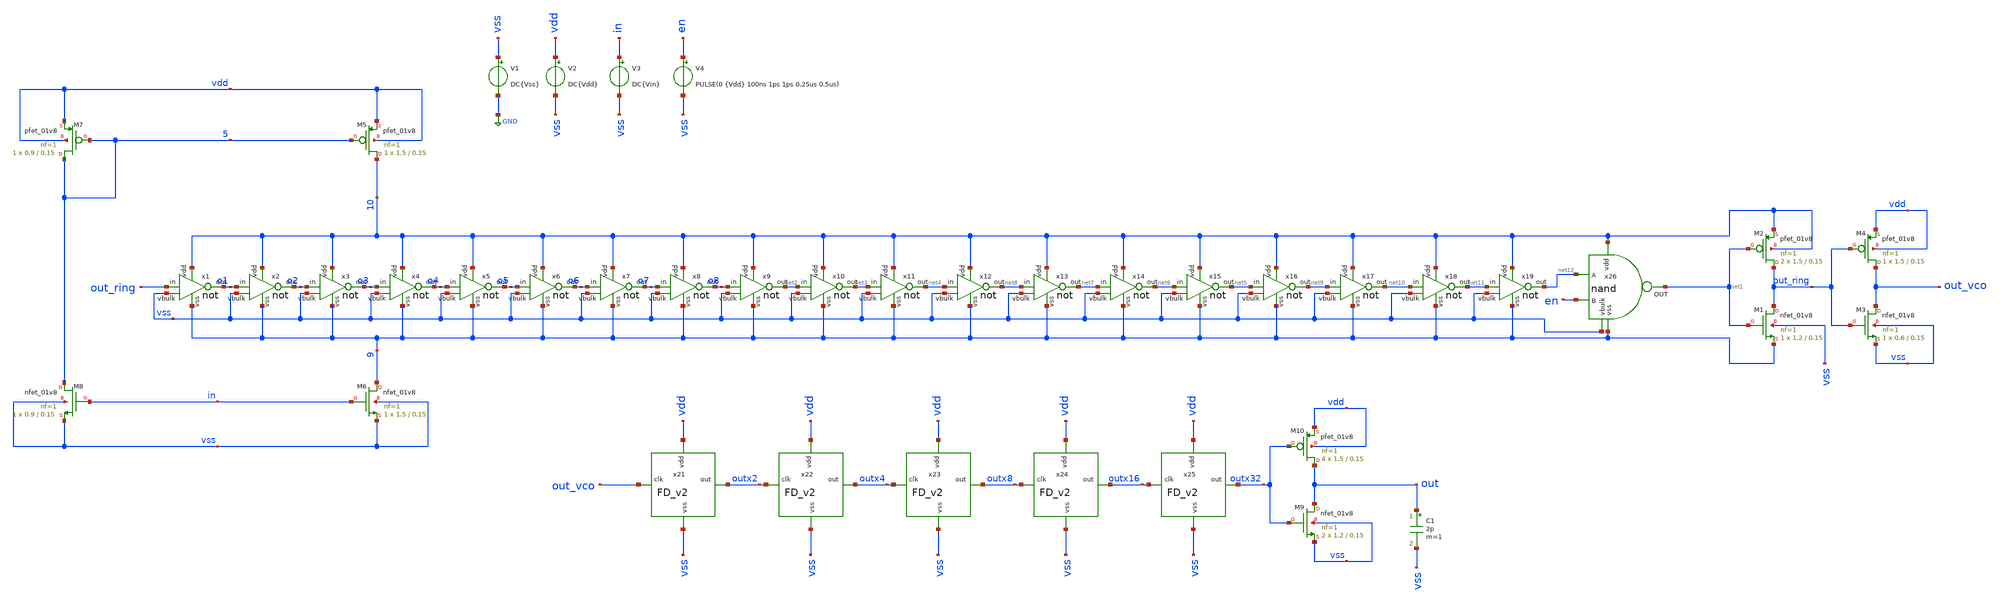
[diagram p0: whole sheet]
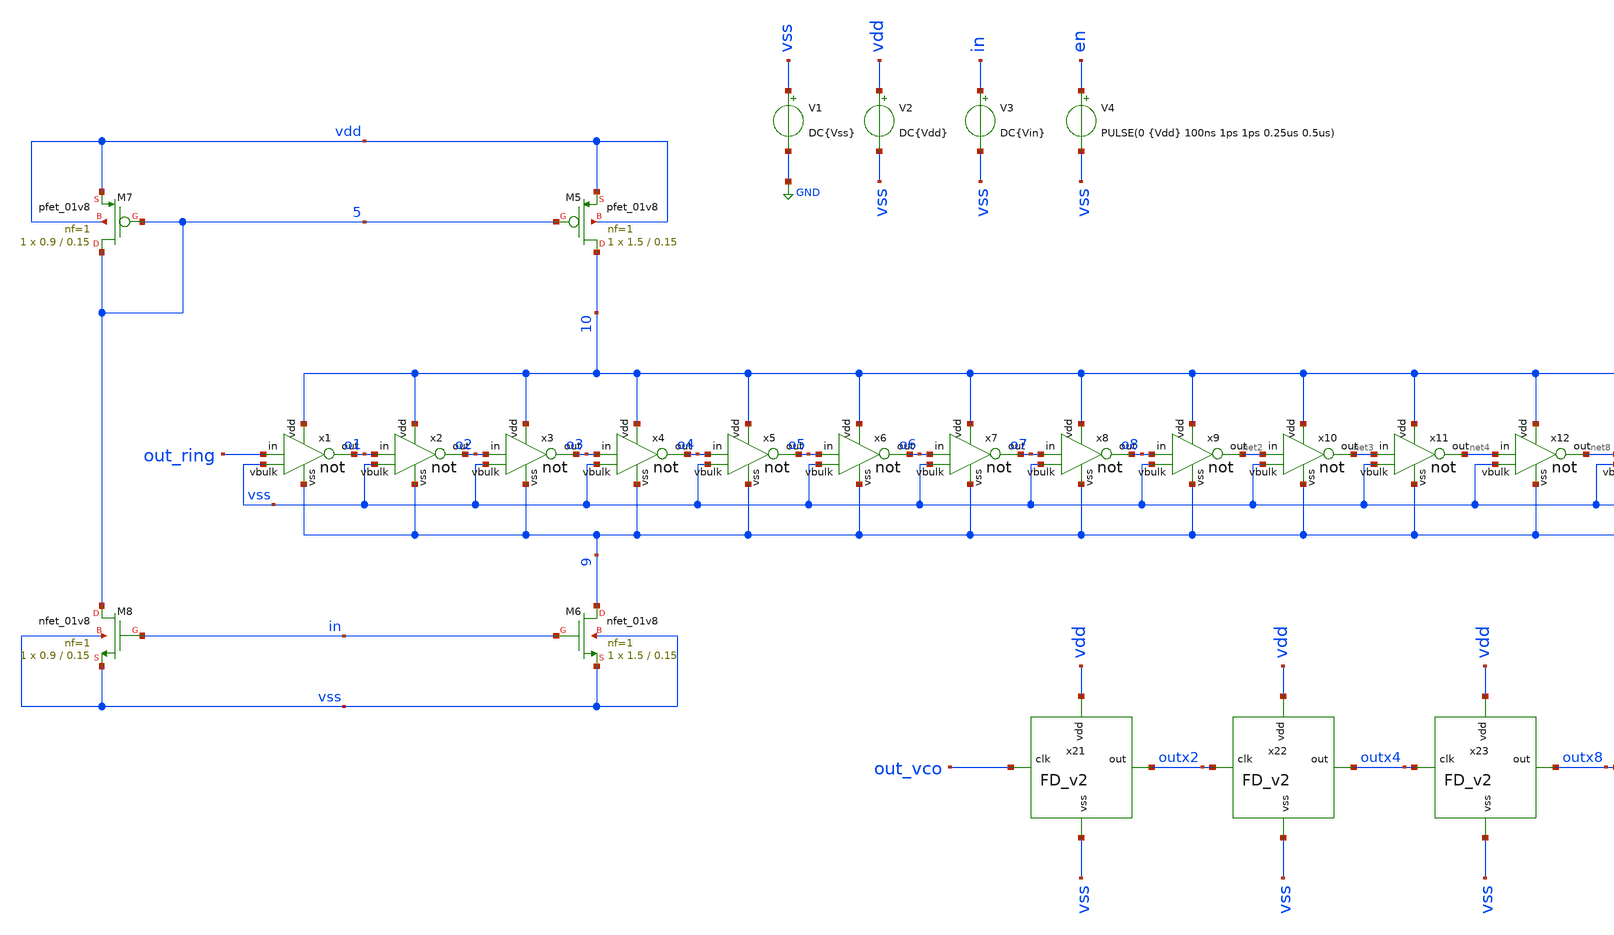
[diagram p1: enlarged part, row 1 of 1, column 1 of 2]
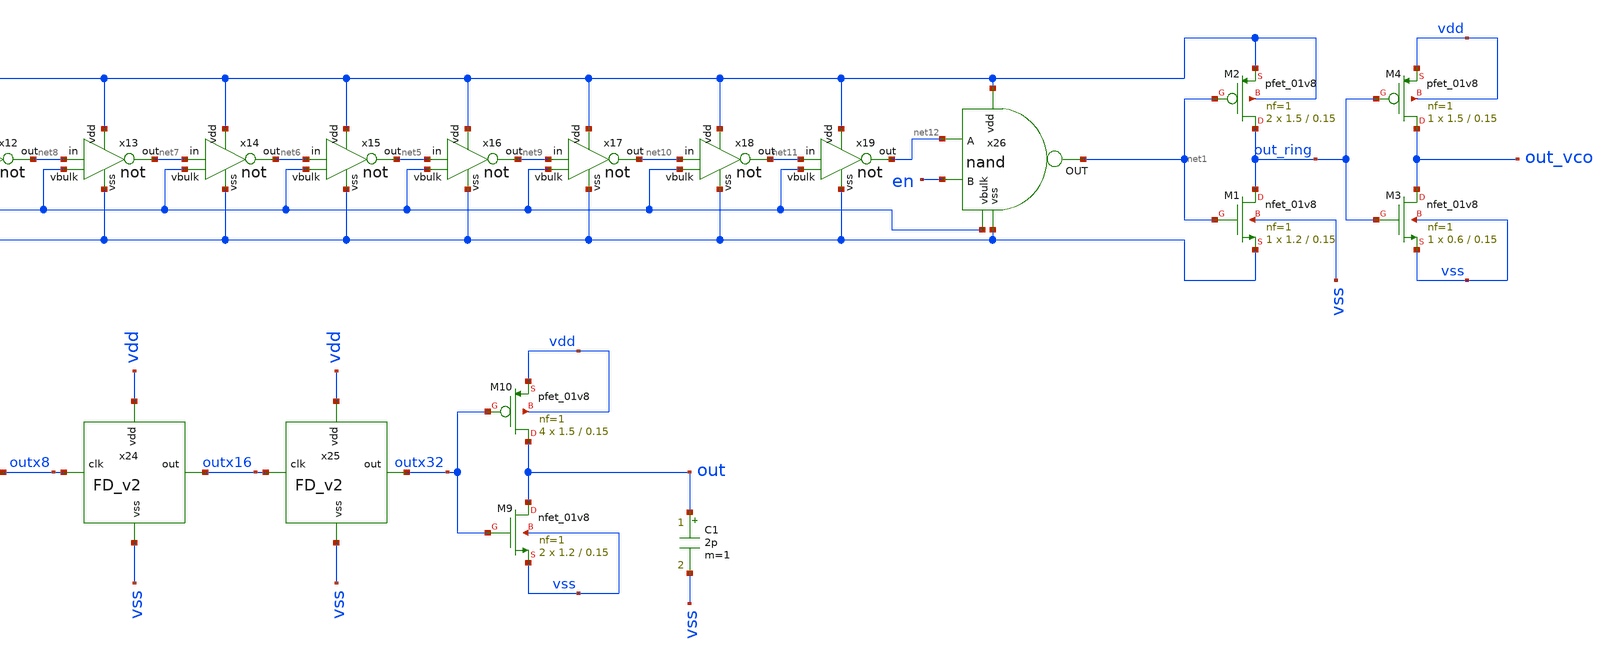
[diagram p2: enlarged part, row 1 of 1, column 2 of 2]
** sch_path: xsch/sch/ring_vco/ring_vco.sch
**.subckt ring_vco
x1 10 out_ring o1 9 vss not
V1 vss GND DC{Vss}
V2 vdd vss DC{Vdd}
x2 10 o1 o2 9 vss not
x3 10 o2 o3 9 vss not
x4 10 o3 o4 9 vss not
x5 10 o4 o5 9 vss not
x6 10 o5 o6 9 vss not
XM1 out_ring net1 9 vss sky130_fd_pr__nfet_01v8 L=0.15 W=1.2 nf=1 ad='W * 0.29' as='W * 0.29' pd='2 * (W + 0.29)'
+ ps='2 * (W + 0.29)' nrd='0.29 / W' nrs='0.29 / W' sa=0 sb=0 sd=0 mult=1 m=1
XM2 out_ring net1 10 10 sky130_fd_pr__pfet_01v8 L=0.15 W=1.5 nf=1 ad='W * 0.29' as='W * 0.29' pd='2 * (W + 0.29)'
+ ps='2 * (W + 0.29)' nrd='0.29 / W' nrs='0.29 / W' sa=0 sb=0 sd=0 mult=2 m=2
XM3 out_vco out_ring vss vss sky130_fd_pr__nfet_01v8 L=0.15 W=0.6 nf=1 ad='W * 0.29' as='W * 0.29' pd='2 * (W + 0.29)'
+ ps='2 * (W + 0.29)' nrd='0.29 / W' nrs='0.29 / W' sa=0 sb=0 sd=0 mult=1 m=1
XM4 out_vco out_ring vdd vdd sky130_fd_pr__pfet_01v8 L=0.15 W=1.5 nf=1 ad='W * 0.29' as='W * 0.29' pd='2 * (W + 0.29)'
+ ps='2 * (W + 0.29)' nrd='0.29 / W' nrs='0.29 / W' sa=0 sb=0 sd=0 mult=1 m=1
XM5 10 5 vdd vdd sky130_fd_pr__pfet_01v8 L=0.15 W=1.5 nf=1 ad='W * 0.29' as='W * 0.29' pd='2 * (W + 0.29)'
+ ps='2 * (W + 0.29)' nrd='0.29 / W' nrs='0.29 / W' sa=0 sb=0 sd=0 mult=1 m=1
XM6 9 in vss vss sky130_fd_pr__nfet_01v8 L=0.15 W=1.5 nf=1 ad='W * 0.29' as='W * 0.29' pd='2 * (W + 0.29)'
+ ps='2 * (W + 0.29)' nrd='0.29 / W' nrs='0.29 / W' sa=0 sb=0 sd=0 mult=1 m=1
XM7 5 5 vdd vdd sky130_fd_pr__pfet_01v8 L=0.15 W=0.9 nf=1 ad='W * 0.29' as='W * 0.29' pd='2 * (W + 0.29)'
+ ps='2 * (W + 0.29)' nrd='0.29 / W' nrs='0.29 / W' sa=0 sb=0 sd=0 mult=1 m=1
XM8 5 in vss vss sky130_fd_pr__nfet_01v8 L=0.15 W=0.9 nf=1 ad='W * 0.29' as='W * 0.29' pd='2 * (W + 0.29)'
+ ps='2 * (W + 0.29)' nrd='0.29 / W' nrs='0.29 / W' sa=0 sb=0 sd=0 mult=1 m=1
V3 in vss DC{Vin}
x7 10 o6 o7 9 vss not
x8 10 o7 o8 9 vss not
x9 10 o8 net2 9 vss not
x10 10 net2 net3 9 vss not
x11 10 net3 net4 9 vss not
x12 10 net4 net8 9 vss not
x13 10 net8 net7 9 vss not
x14 10 net7 net6 9 vss not
x15 10 net6 net5 9 vss not
x16 10 net5 net9 9 vss not
x17 10 net9 net10 9 vss not
x18 10 net10 net11 9 vss not
x19 10 net11 net12 9 vss not
x21 out_vco vss outx2 vdd FD_v2
x22 outx2 vss outx4 vdd FD_v2
x23 outx4 vss outx8 vdd FD_v2
x24 outx8 vss outx16 vdd FD_v2
x25 outx16 vss outx32 vdd FD_v2
C1 out vss 2p m=1
XM9 out outx32 vss vss sky130_fd_pr__nfet_01v8 L=0.15 W=1.2 nf=1 ad='W * 0.29' as='W * 0.29' pd='2 * (W + 0.29)'
+ ps='2 * (W + 0.29)' nrd='0.29 / W' nrs='0.29 / W' sa=0 sb=0 sd=0 mult=2 m=2
XM10 out outx32 vdd vdd sky130_fd_pr__pfet_01v8 L=0.15 W=1.5 nf=1 ad='W * 0.29' as='W * 0.29' pd='2 * (W + 0.29)'
+ ps='2 * (W + 0.29)' nrd='0.29 / W' nrs='0.29 / W' sa=0 sb=0 sd=0 mult=4 m=4
x26 10 net12 net1 en 9 vss nand
V4 en vss PULSE(0 {Vdd} 100ns 1ps 1ps 0.25us 0.5us)
**** begin user architecture code




* Circuit Parameters
.param vdd  = 1.8
.param vss  = 0.0
.param vin  = 1
.param iref = 200u
.options TEMP = 65.0

* Include Models
.lib /home/tools/repos_sky130/skywater-pdk/libraries/sky130_fd_pr_ngspice/latest/models/corners/sky130.lib TT

* OP Parameters & Singals to save
.save all  @M.X2.XM1.msky130_fd_pr__nfet_01v8[id] @M.X2.XM1.msky130_fd_pr__nfet_01v8[vth] @M.X2.XM1.msky130_fd_pr__nfet_01v8[vgs] @M.X2.XM1.msky130_fd_pr__nfet_01v8[vds] @M.X2.XM1.msky130_fd_pr__nfet_01v8[vdsat] @M.X2.XM1.msky130_fd_pr__nfet_01v8[gm] @M.X2.XM1.msky130_fd_pr__nfet_01v8[gds] @M.X2.XM1.msky130_fd_pr__nfet_01v8[cgs] @M.X2.XM1.msky130_fd_pr__nfet_01v8[cgd]  @M.X2.XM2.msky130_fd_pr__pfet_01v8[id] @M.X2.XM2.msky130_fd_pr__pfet_01v8[vth] @M.X2.XM2.msky130_fd_pr__pfet_01v8[vgs] @M.X2.XM2.msky130_fd_pr__pfet_01v8[vds] @M.X2.XM2.msky130_fd_pr__pfet_01v8[vdsat] @M.X2.XM2.msky130_fd_pr__pfet_01v8[gm] @M.X2.XM2.msky130_fd_pr__pfet_01v8[gds] @M.X2.XM1.msky130_fd_pr__nfet_01v8[cgs] @M.X2.XM1.msky130_fd_pr__nfet_01v8[cgd]  @M.XM6.msky130_fd_pr__nfet_01v8[id] @M.XM6.msky130_fd_pr__nfet_01v8[vth] @M.XM6.msky130_fd_pr__nfet_01v8[vgs] @M.XM6.msky130_fd_pr__nfet_01v8[vds] @M.XM6.msky130_fd_pr__nfet_01v8[vdsat] @M.XM6.msky130_fd_pr__nfet_01v8[gm] @M.XM6.msky130_fd_pr__nfet_01v8[gds] @M.XM6.msky130_fd_pr__nfet_01v8[cgs] @M.XM6.msky130_fd_pr__nfet_01v8[cgd]  @M.XM5.msky130_fd_pr__pfet_01v8[id] @M.XM5.msky130_fd_pr__pfet_01v8[vth] @M.XM5.msky130_fd_pr__pfet_01v8[vgs] @M.XM5.msky130_fd_pr__pfet_01v8[vds] @M.XM5.msky130_fd_pr__pfet_01v8[vdsat] @M.XM5.msky130_fd_pr__pfet_01v8[gm] @M.XM5.msky130_fd_pr__pfet_01v8[gds] @M.XM5.msky130_fd_pr__nfet_01v8[cgs] @M.XM5.msky130_fd_pr__nfet_01v8[cgd]



*Simulations
.control
  tran 0.05n 1u
  setplot tran1
  plot v(out) v(outx32)+2 v(outx16)+4 v(outx8)+6 v(outx4)+8 v(outx2)+10 v(out_vco)+12 v(en)+14

  linearize
  set specwindow=blackman
  fft v(out_vco)
  spec 10 1000000 1000 v(out_vco)
  plot mag(v(out_vco))

  reset
  tran 0.05n 1u
  setplot tran2
  linearize
  fft v(out)
  spec 10 1000000 1000 v(out)
  plot mag(v(out))
  write ~/caravel_fulgor_opamp/xschem/ring_vco/sim_results/ring_vco_tran1.raw


.endc

.end


**** end user architecture code
**.ends
.GLOBAL GND
.end
